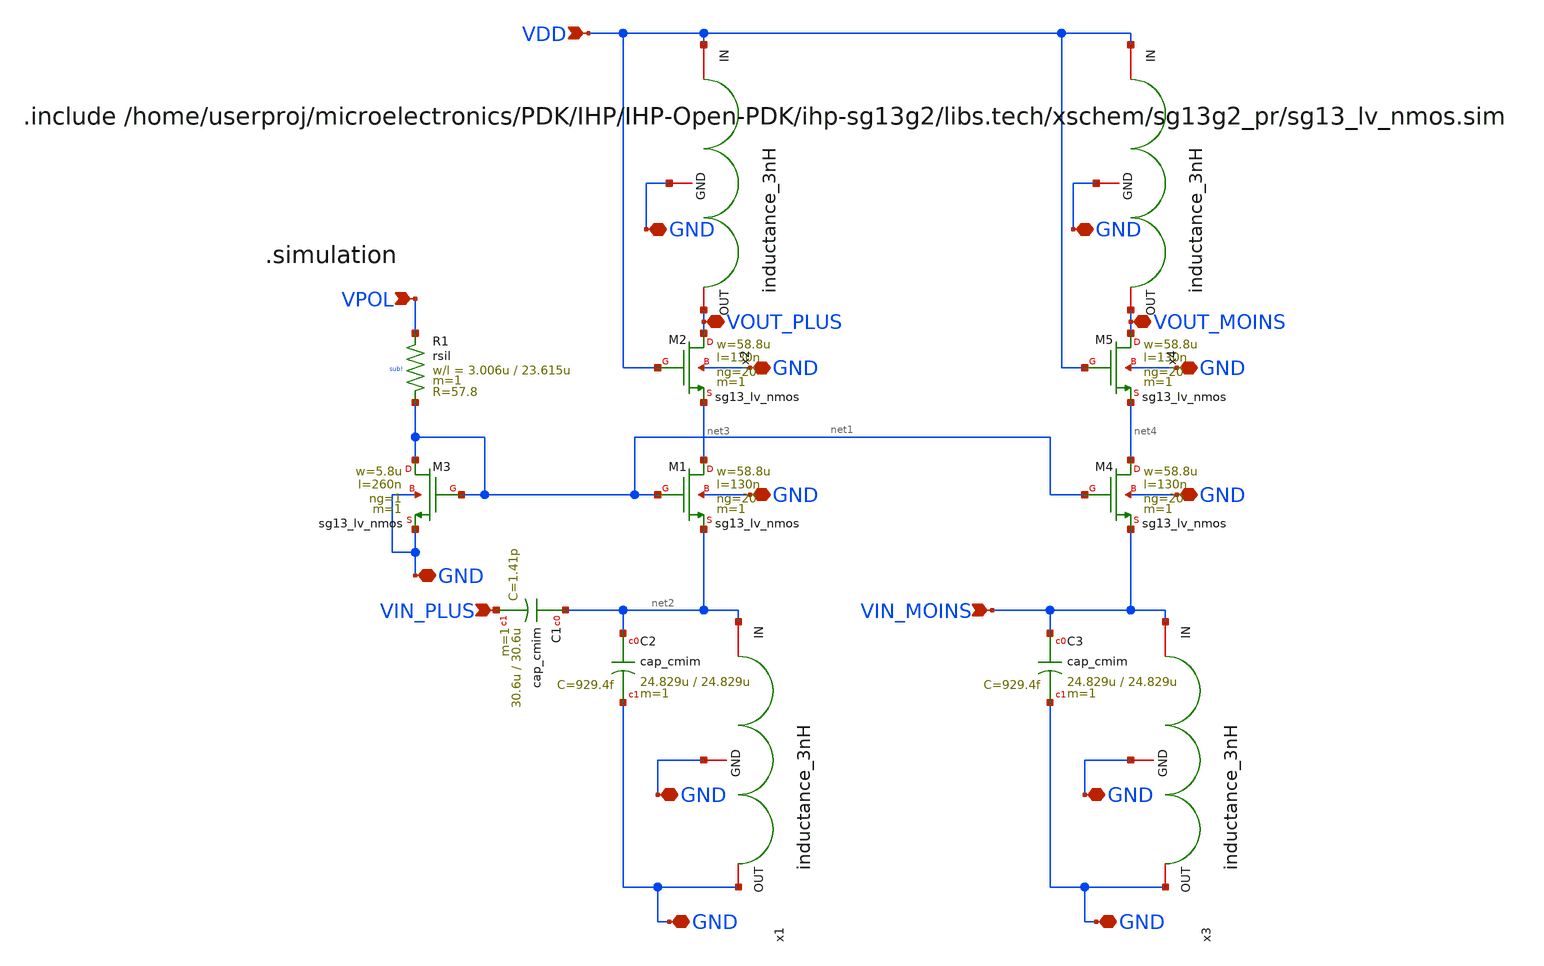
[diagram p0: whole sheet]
** sch_path: LVS/xschem/BGM_AA/LNA_GC_DIFF/TOP.sch
**.subckt TOP VIN_PLUS GND VDD VPOL GND GND GND GND GND VOUT_PLUS GND GND GND GND GND VOUT_MOINS
*+ VIN_MOINS
*.ipin VIN_PLUS
*.iopin GND
*.ipin VDD
*.ipin VPOL
*.iopin GND
*.iopin GND
*.iopin GND
*.iopin GND
*.iopin GND
*.iopin VOUT_PLUS
*.iopin GND
*.iopin GND
*.iopin GND
*.iopin GND
*.iopin GND
*.iopin VOUT_MOINS
*.ipin VIN_MOINS
XM1 net3 net1 net2 GND sg13_lv_nmos w=58.8u l=130n ng=20 m=1 mm_ok=1
XR1 VPOL net1 sub! rsil w=3.006u l=23.615u m=1 mm_ok=1
XM3 net1 net1 GND GND sg13_lv_nmos w=5.8u l=260n ng=1 m=1 mm_ok=1
XM2 VOUT_PLUS VDD net3 GND sg13_lv_nmos w=58.8u l=130n ng=20 m=1 mm_ok=1
XC1 net2 VIN_PLUS cap_cmim w=30.6u l=30.6u m=1 mm_ok=1
XC2 net2 GND cap_cmim w=24.829u l=24.829u m=1 mm_ok=1
x1 GND net2 GND inductance_3nH
x2 VOUT_PLUS VDD GND inductance_3nH
XM4 net4 net1 VIN_MOINS GND sg13_lv_nmos w=58.8u l=130n ng=20 m=1 mm_ok=1
XM5 VOUT_MOINS VDD net4 GND sg13_lv_nmos w=58.8u l=130n ng=20 m=1 mm_ok=1
XC3 VIN_MOINS GND cap_cmim w=24.829u l=24.829u m=1 mm_ok=1
x3 GND VIN_MOINS GND inductance_3nH
x4 VOUT_MOINS VDD GND inductance_3nH
**.ends

* expanding   symbol:
*+  /home/userproj/microelectronics/projects/ZigBee/Inductance/MODEL_XSCHEM/inductance_3nH.sym # of pins=3
** sym_path: Inductance/MODEL_XSCHEM/inductance_3nH.sym
** sch_path: Inductance/MODEL_XSCHEM/inductance_3nH.sch
.subckt inductance_3nH OUT IN GND
*.iopin GND
*.iopin OUT
*.iopin IN
Ls net1 OUT 2.885n m=1
Cox1 IN net2 55.8f m=1
Cox2 OUT net3 55.8f m=1
Csp IN OUT 13.69f m=1
Rp1 net2 GND 18.32 m=1
Rp2 net3 GND 18.32 m=1
Rs IN net1 3.623 m=1
.ends

.end
